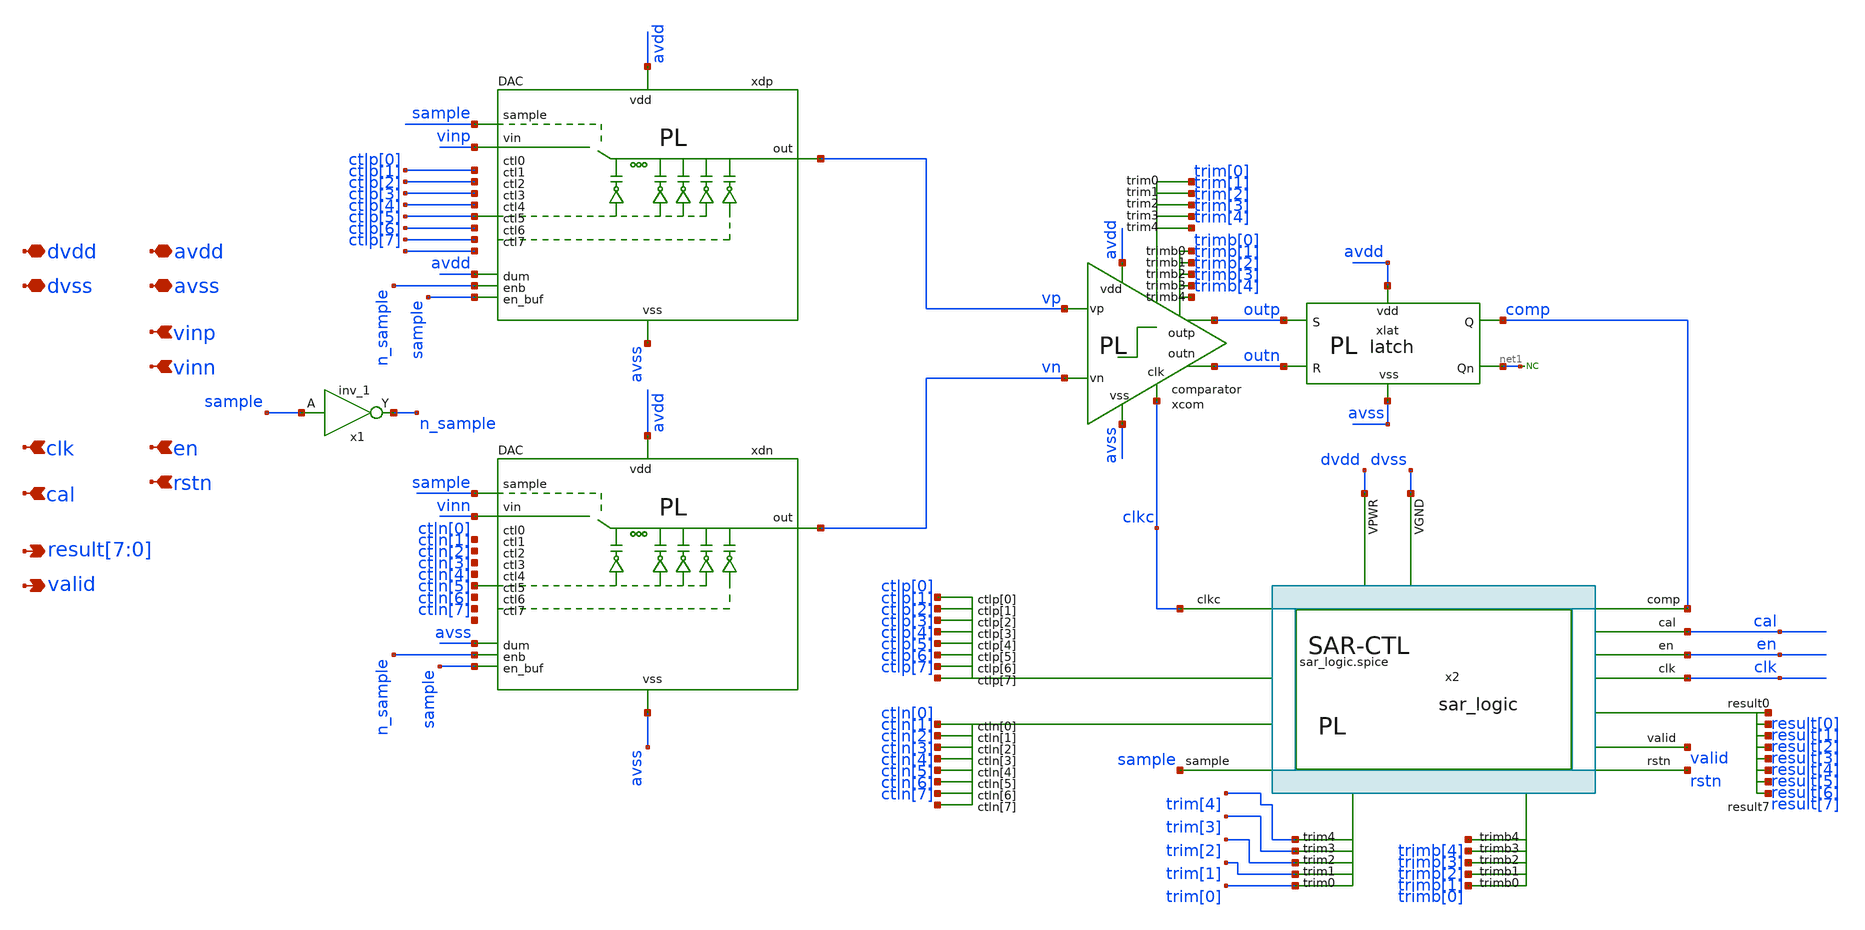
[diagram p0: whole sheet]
** sch_path: full_ext_sim/sar/sar_post/sar_post.sch
**.subckt sar_post avss avdd dvss dvdd vinp vinn
*+ result[7],result[6],result[5],result[4],result[3],result[2],result[1],result[0] clk en valid cal rstn
*.iopin avss
*.iopin avdd
*.iopin dvss
*.iopin dvdd
*.ipin vinp
*.ipin vinn
*.opin result[7],result[6],result[5],result[4],result[3],result[2],result[1],result[0]
*.ipin clk
*.ipin en
*.opin valid
*.ipin cal
*.ipin rstn
xlat avdd avss net1 outp outn comp latch
* noconn #net1
xdn n_sample sample ctln[1] ctln[0] avss ctln[3] ctln[4] ctln[5] ctln[6] ctln[7] ctln[2] avdd avss
+ sample vn vinn DAC
xcom trim[3] trim[2] trim[0] trim[1] trim[4] trimb[4] trimb[1] trimb[0] trimb[2] trimb[3] outn outp
+ clkc avdd avss vn vp comparator
xdp n_sample sample ctlp[1] ctlp[0] avdd ctlp[3] ctlp[4] ctlp[5] ctlp[6] ctlp[7] ctlp[2] avdd avss
+ sample vp vinp DAC
x1 sample VGND VNB VPB VPWR n_sample sky130_fd_sc_hd__inv_1
x2 dvss dvdd cal clk clkc comp ctln[0] ctln[1] ctln[2] ctln[3] ctln[4] ctln[5] ctln[6] ctln[7]
+ ctlp[0] ctlp[1] ctlp[2] ctlp[3] ctlp[4] ctlp[5] ctlp[6] ctlp[7] en result[0] result[1] result[2] result[3]
+ result[4] result[5] result[6] result[7] rstn sample trim[0] trim[1] trim[2] trim[3] trim[4] trimb[0] trimb[1]
+ trimb[2] trimb[3] trimb[4] valid sar_logic
**.ends
.end
